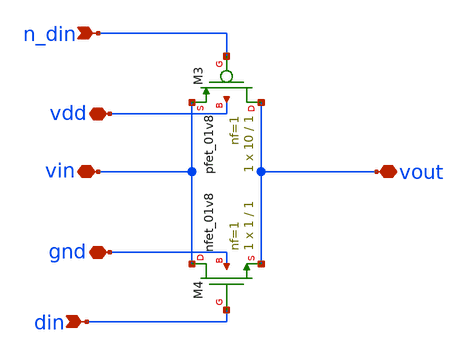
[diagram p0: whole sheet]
** sch_path: Symbols/tranmission_gates.sch
**.subckt tranmission_gates din n_din vdd gnd vin vout
*.ipin din
*.ipin n_din
*.iopin vdd
*.iopin gnd
*.iopin vin
*.iopin vout
XM3 vout n_din vin vdd sky130_fd_pr__pfet_01v8 L=1 W=10 nf=1 ad='int((nf+1)/2) * W/nf * 0.29' as='int((nf+2)/2) * W/nf * 0.29'
+ pd='2*int((nf+1)/2) * (W/nf + 0.29)' ps='2*int((nf+2)/2) * (W/nf + 0.29)' nrd='0.29 / W' nrs='0.29 / W'
+ sa=0 sb=0 sd=0 mult=1 m=1
XM4 vin din vout gnd sky130_fd_pr__nfet_01v8 L=1 W=1 nf=1 ad='int((1 + 1)/2) * 1 / 1 * 0.29' as='int((1 + 2)/2) * 1 / 1 * 0.29'
+ pd='2*int((1 + 1)/2) * (1 / 1 + 0.29)' ps='2*int((1 + 2)/2) * (1 / 1 + 0.29)' nrd='0.29 / 1 ' nrs='0.29 / 1 '
+ sa=0 sb=0 sd=0 mult=1 m=1
**.ends
.end
